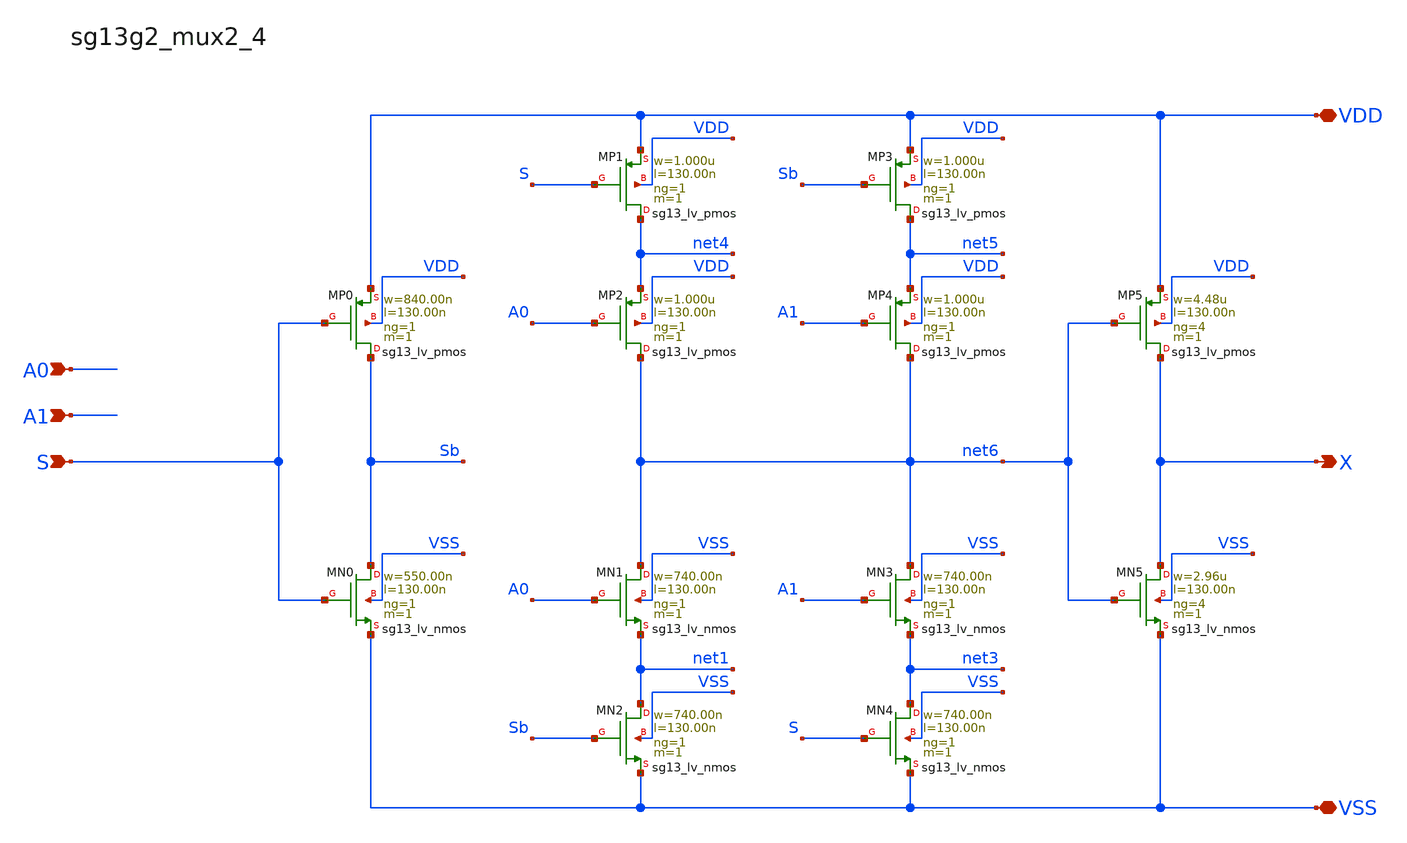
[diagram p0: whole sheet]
** sch_path: outputs/sg13g2_cells/cells/sg13g2_mux2_4/sg13g2_mux2_4.sch
**.subckt sg13g2_mux2_4 X A0 A1 S VDD VSS
*.opin X
*.ipin A0
*.ipin A1
*.ipin S
*.iopin VDD
*.iopin VSS
XMP1 net4 S VDD VDD sg13_lv_pmos w=1.000u l=130.00n ng=1 m=1 mm_ok=1
XMP5 X net6 VDD VDD sg13_lv_pmos w=4.48u l=130.00n ng=4 m=1 mm_ok=1
XMP4 net6 A1 net5 VDD sg13_lv_pmos w=1.000u l=130.00n ng=1 m=1 mm_ok=1
XMP0 Sb S VDD VDD sg13_lv_pmos w=840.00n l=130.00n ng=1 m=1 mm_ok=1
XMP3 net5 Sb VDD VDD sg13_lv_pmos w=1.000u l=130.00n ng=1 m=1 mm_ok=1
XMP2 net6 A0 net4 VDD sg13_lv_pmos w=1.000u l=130.00n ng=1 m=1 mm_ok=1
XMN4 net3 S VSS VSS sg13_lv_nmos w=740.00n l=130.00n ng=1 m=1 mm_ok=1
XMN2 net1 Sb VSS VSS sg13_lv_nmos w=740.00n l=130.00n ng=1 m=1 mm_ok=1
XMN5 X net6 VSS VSS sg13_lv_nmos w=2.96u l=130.00n ng=4 m=1 mm_ok=1
XMN0 Sb S VSS VSS sg13_lv_nmos w=550.00n l=130.00n ng=1 m=1 mm_ok=1
XMN3 net6 A1 net3 VSS sg13_lv_nmos w=740.00n l=130.00n ng=1 m=1 mm_ok=1
XMN1 net6 A0 net1 VSS sg13_lv_nmos w=740.00n l=130.00n ng=1 m=1 mm_ok=1
**.ends
.end
